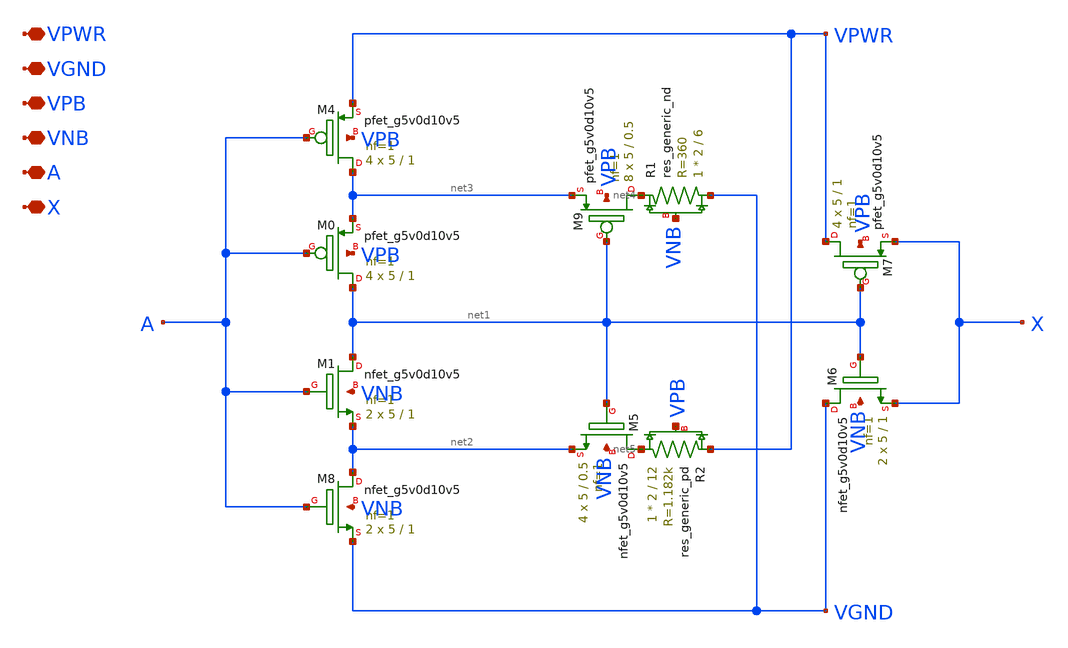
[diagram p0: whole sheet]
** sch_path: images/iic-osic-tools/addons/examples/open-pmic/design/oscillator/schmittbuf.sch
**.subckt schmittbuf VPWR VGND VPB VNB A X
*.iopin VPWR
*.iopin VGND
*.iopin VPB
*.iopin VNB
*.iopin A
*.iopin X
XM1 net1 A net2 VNB sky130_fd_pr__nfet_g5v0d10v5 L=1 W=5 nf=1 ad='int((nf+1)/2) * W/nf * 0.29' as='int((nf+2)/2) * W/nf * 0.29'
+ pd='2*int((nf+1)/2) * (W/nf + 0.29)' ps='2*int((nf+2)/2) * (W/nf + 0.29)' nrd='0.29 / W' nrs='0.29 / W'
+ sa=0 sb=0 sd=0 mult=2 m=2
XM8 net2 A VGND VNB sky130_fd_pr__nfet_g5v0d10v5 L=1 W=5 nf=1 ad='int((nf+1)/2) * W/nf * 0.29' as='int((nf+2)/2) * W/nf * 0.29'
+ pd='2*int((nf+1)/2) * (W/nf + 0.29)' ps='2*int((nf+2)/2) * (W/nf + 0.29)' nrd='0.29 / W' nrs='0.29 / W'
+ sa=0 sb=0 sd=0 mult=2 m=2
XM0 net1 A net3 VPB sky130_fd_pr__pfet_g5v0d10v5 L=1 W=5 nf=1 ad='int((nf+1)/2) * W/nf * 0.29' as='int((nf+2)/2) * W/nf * 0.29'
+ pd='2*int((nf+1)/2) * (W/nf + 0.29)' ps='2*int((nf+2)/2) * (W/nf + 0.29)' nrd='0.29 / W' nrs='0.29 / W'
+ sa=0 sb=0 sd=0 mult=4 m=4
XM4 net3 A VPWR VPB sky130_fd_pr__pfet_g5v0d10v5 L=1 W=5 nf=1 ad='int((nf+1)/2) * W/nf * 0.29' as='int((nf+2)/2) * W/nf * 0.29'
+ pd='2*int((nf+1)/2) * (W/nf + 0.29)' ps='2*int((nf+2)/2) * (W/nf + 0.29)' nrd='0.29 / W' nrs='0.29 / W'
+ sa=0 sb=0 sd=0 mult=4 m=4
XM7 VPWR net1 X VPB sky130_fd_pr__pfet_g5v0d10v5 L=1 W=5 nf=1 ad='int((nf+1)/2) * W/nf * 0.29' as='int((nf+2)/2) * W/nf * 0.29'
+ pd='2*int((nf+1)/2) * (W/nf + 0.29)' ps='2*int((nf+2)/2) * (W/nf + 0.29)' nrd='0.29 / W' nrs='0.29 / W'
+ sa=0 sb=0 sd=0 mult=4 m=4
XM6 VGND net1 X VNB sky130_fd_pr__nfet_g5v0d10v5 L=1 W=5 nf=1 ad='int((nf+1)/2) * W/nf * 0.29' as='int((nf+2)/2) * W/nf * 0.29'
+ pd='2*int((nf+1)/2) * (W/nf + 0.29)' ps='2*int((nf+2)/2) * (W/nf + 0.29)' nrd='0.29 / W' nrs='0.29 / W'
+ sa=0 sb=0 sd=0 mult=2 m=2
XM9 net4 net1 net3 VPB sky130_fd_pr__pfet_g5v0d10v5 L=0.5 W=5 nf=1 ad='int((nf+1)/2) * W/nf * 0.29' as='int((nf+2)/2) * W/nf * 0.29'
+ pd='2*int((nf+1)/2) * (W/nf + 0.29)' ps='2*int((nf+2)/2) * (W/nf + 0.29)' nrd='0.29 / W' nrs='0.29 / W'
+ sa=0 sb=0 sd=0 mult=8 m=8
XM5 net5 net1 net2 VNB sky130_fd_pr__nfet_g5v0d10v5 L=0.5 W=5 nf=1 ad='int((nf+1)/2) * W/nf * 0.29' as='int((nf+2)/2) * W/nf * 0.29'
+ pd='2*int((nf+1)/2) * (W/nf + 0.29)' ps='2*int((nf+2)/2) * (W/nf + 0.29)' nrd='0.29 / W' nrs='0.29 / W'
+ sa=0 sb=0 sd=0 mult=4 m=4
XR1 VGND net4 VNB sky130_fd_pr__res_generic_nd W=2 L=6 mult=1 m=1
XR2 net5 VPWR VPB sky130_fd_pr__res_generic_pd W=2 L=12 mult=1 m=1
**.ends
.end
